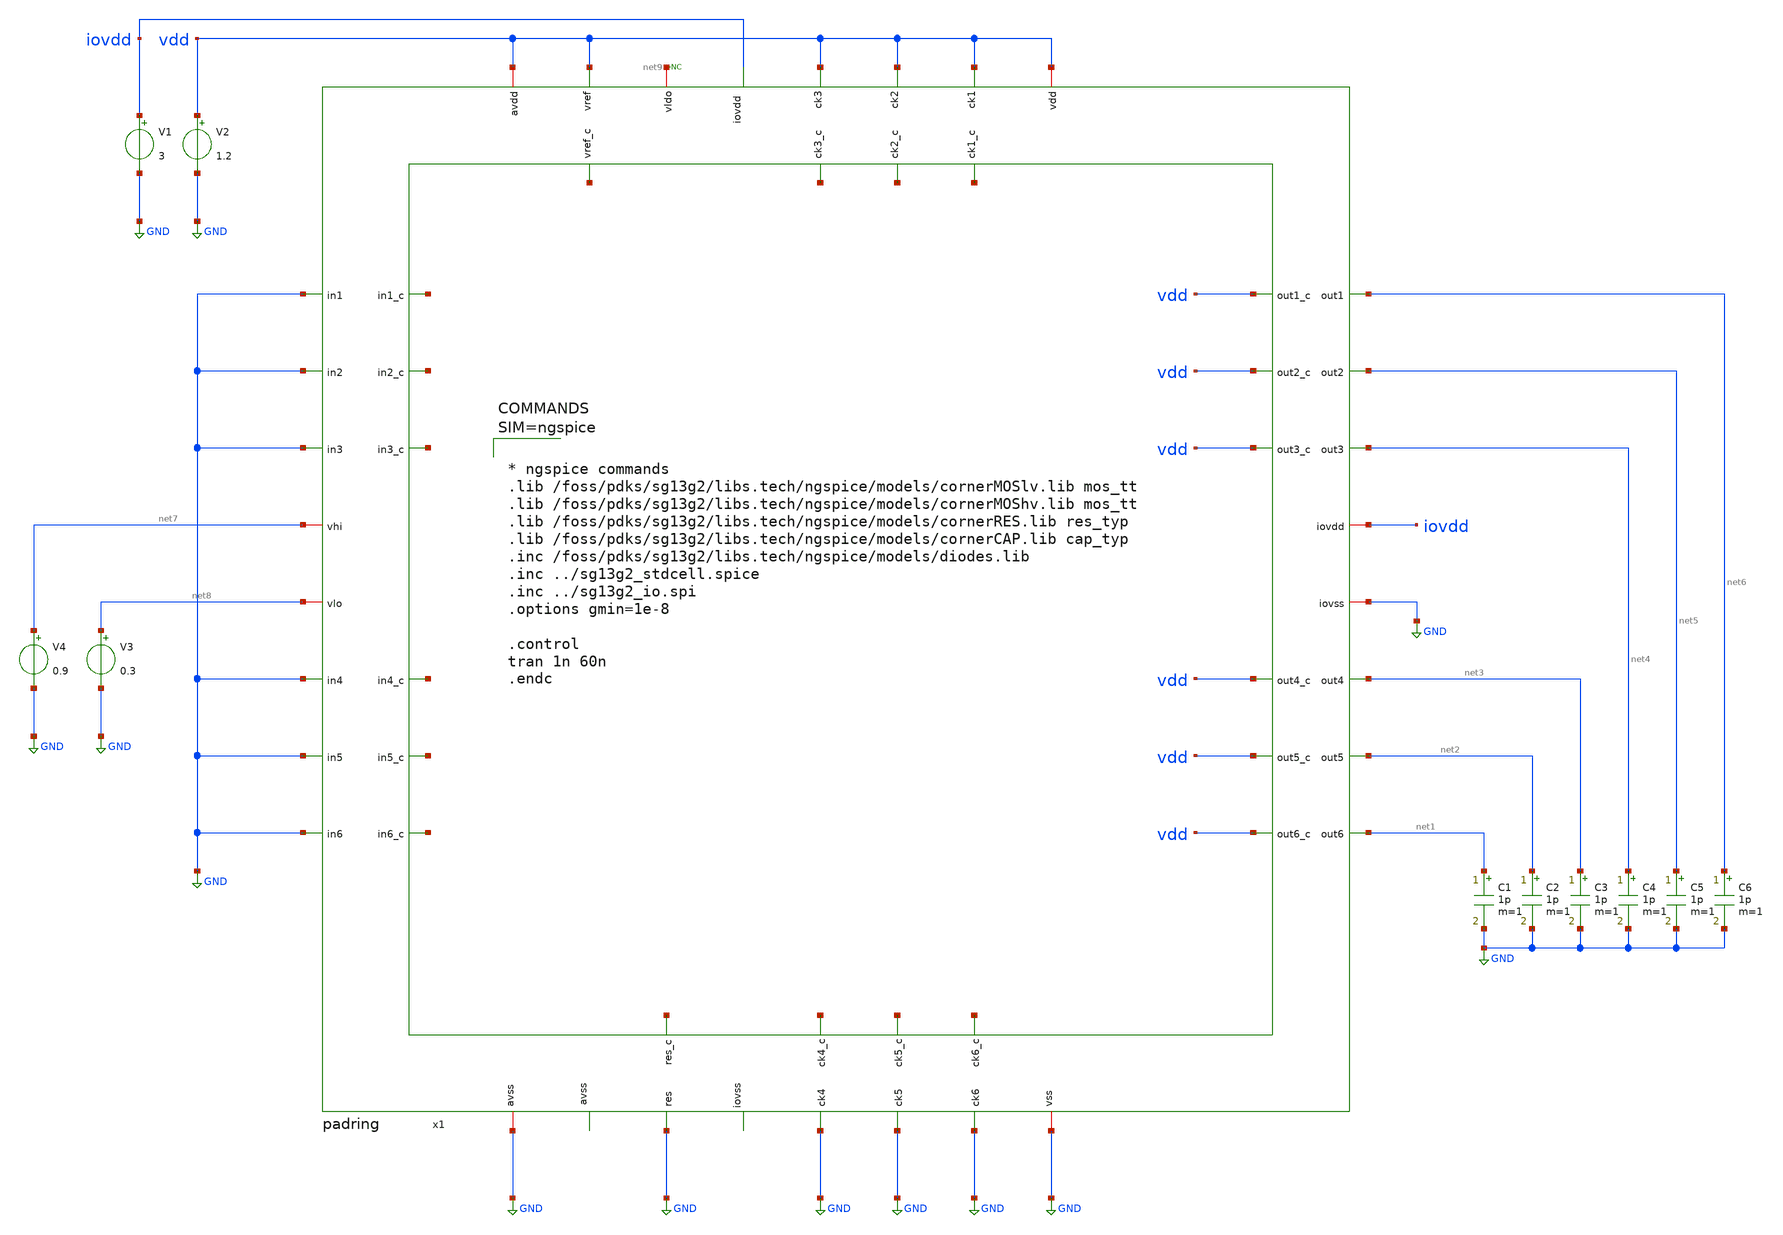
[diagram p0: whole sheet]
** sch_path: 5_Design/3_Real_circuits/tb_padring.sch
**.subckt tb_padring
V1 iovdd GND 3
V2 vdd GND 1.2
* noconn #net9
V3 net8 GND 0.3
V4 net7 GND 0.9
C1 net1 GND 1p m=1
C2 net2 GND 1p m=1
C3 net3 GND 1p m=1
C4 net4 GND 1p m=1
C5 net5 GND 1p m=1
C6 net6 GND 1p m=1
x1 vdd vdd net9 vdd vdd net10 net11 net12 net13 vdd GND net6 GND net5 vdd net14 vdd net4 net15 GND
+ vdd vdd iovdd net7 GND GND net8 net3 net16 GND vdd net2 net17 vdd GND GND net18 net1 vdd net19 net20
+ net21 net22 GND GND GND GND net23 GND padring
**** begin user architecture code



* ngspice commands
.lib /foss/pdks/sg13g2/libs.tech/ngspice/models/cornerMOSlv.lib mos_tt
.lib /foss/pdks/sg13g2/libs.tech/ngspice/models/cornerMOShv.lib mos_tt
.lib /foss/pdks/sg13g2/libs.tech/ngspice/models/cornerRES.lib res_typ
.lib /foss/pdks/sg13g2/libs.tech/ngspice/models/cornerCAP.lib cap_typ
.inc /foss/pdks/sg13g2/libs.tech/ngspice/models/diodes.lib
.inc ../sg13g2_stdcell.spice
.inc ../sg13g2_io.spi
.options gmin=1e-8

.control
tran 1n 60n
.endc


**** end user architecture code
**.ends
.GLOBAL GND
.end
